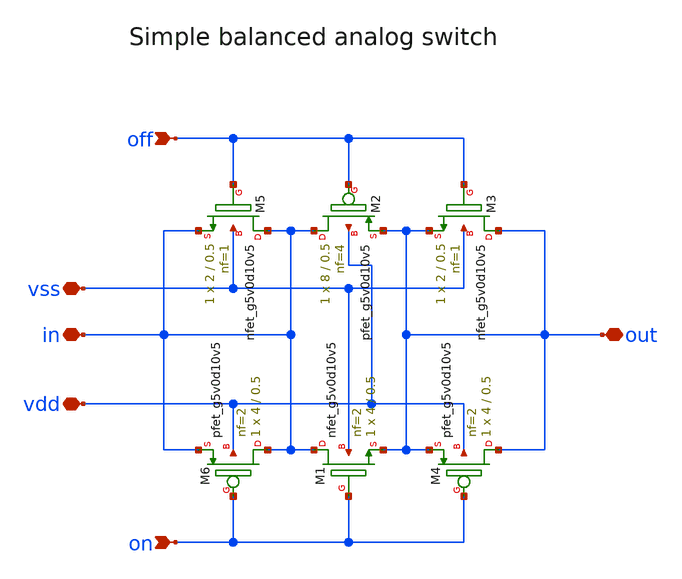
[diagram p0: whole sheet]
** sch_path: analog/repairs/cdac_tap_baseline/project/dependencies/sky130_ef_ip__analog_switches/xschem/simple_analog_switch.sch
**.subckt simple_analog_switch on out vdd vss in off
*.ipin on
*.iopin out
*.iopin vdd
*.iopin vss
*.iopin in
*.ipin off
XM1 in on out vss sky130_fd_pr__nfet_g5v0d10v5 L=0.5 W=4 nf=2 ad='int((nf+1)/2) * W/nf * 0.29' as='int((nf+2)/2) * W/nf * 0.29'
+ pd='2*int((nf+1)/2) * (W/nf + 0.29)' ps='2*int((nf+2)/2) * (W/nf + 0.29)' nrd='0.29 / W' nrs='0.29 / W'
+ sa=0 sb=0 sd=0 mult=1 m=1
XM2 in off out vdd sky130_fd_pr__pfet_g5v0d10v5 L=0.5 W=8 nf=4 ad='int((nf+1)/2) * W/nf * 0.29' as='int((nf+2)/2) * W/nf * 0.29'
+ pd='2*int((nf+1)/2) * (W/nf + 0.29)' ps='2*int((nf+2)/2) * (W/nf + 0.29)' nrd='0.29 / W' nrs='0.29 / W'
+ sa=0 sb=0 sd=0 mult=1 m=1
XM3 out off out vss sky130_fd_pr__nfet_g5v0d10v5 L=0.5 W=2 nf=1 ad='int((nf+1)/2) * W/nf * 0.29' as='int((nf+2)/2) * W/nf * 0.29'
+ pd='2*int((nf+1)/2) * (W/nf + 0.29)' ps='2*int((nf+2)/2) * (W/nf + 0.29)' nrd='0.29 / W' nrs='0.29 / W'
+ sa=0 sb=0 sd=0 mult=1 m=1
XM4 out on out vdd sky130_fd_pr__pfet_g5v0d10v5 L=0.5 W=4 nf=2 ad='int((nf+1)/2) * W/nf * 0.29' as='int((nf+2)/2) * W/nf * 0.29'
+ pd='2*int((nf+1)/2) * (W/nf + 0.29)' ps='2*int((nf+2)/2) * (W/nf + 0.29)' nrd='0.29 / W' nrs='0.29 / W'
+ sa=0 sb=0 sd=0 mult=1 m=1
XM5 in off in vss sky130_fd_pr__nfet_g5v0d10v5 L=0.5 W=2 nf=1 ad='int((nf+1)/2) * W/nf * 0.29' as='int((nf+2)/2) * W/nf * 0.29'
+ pd='2*int((nf+1)/2) * (W/nf + 0.29)' ps='2*int((nf+2)/2) * (W/nf + 0.29)' nrd='0.29 / W' nrs='0.29 / W'
+ sa=0 sb=0 sd=0 mult=1 m=1
XM6 in on in vdd sky130_fd_pr__pfet_g5v0d10v5 L=0.5 W=4 nf=2 ad='int((nf+1)/2) * W/nf * 0.29' as='int((nf+2)/2) * W/nf * 0.29'
+ pd='2*int((nf+1)/2) * (W/nf + 0.29)' ps='2*int((nf+2)/2) * (W/nf + 0.29)' nrd='0.29 / W' nrs='0.29 / W'
+ sa=0 sb=0 sd=0 mult=1 m=1
**.ends
.end
